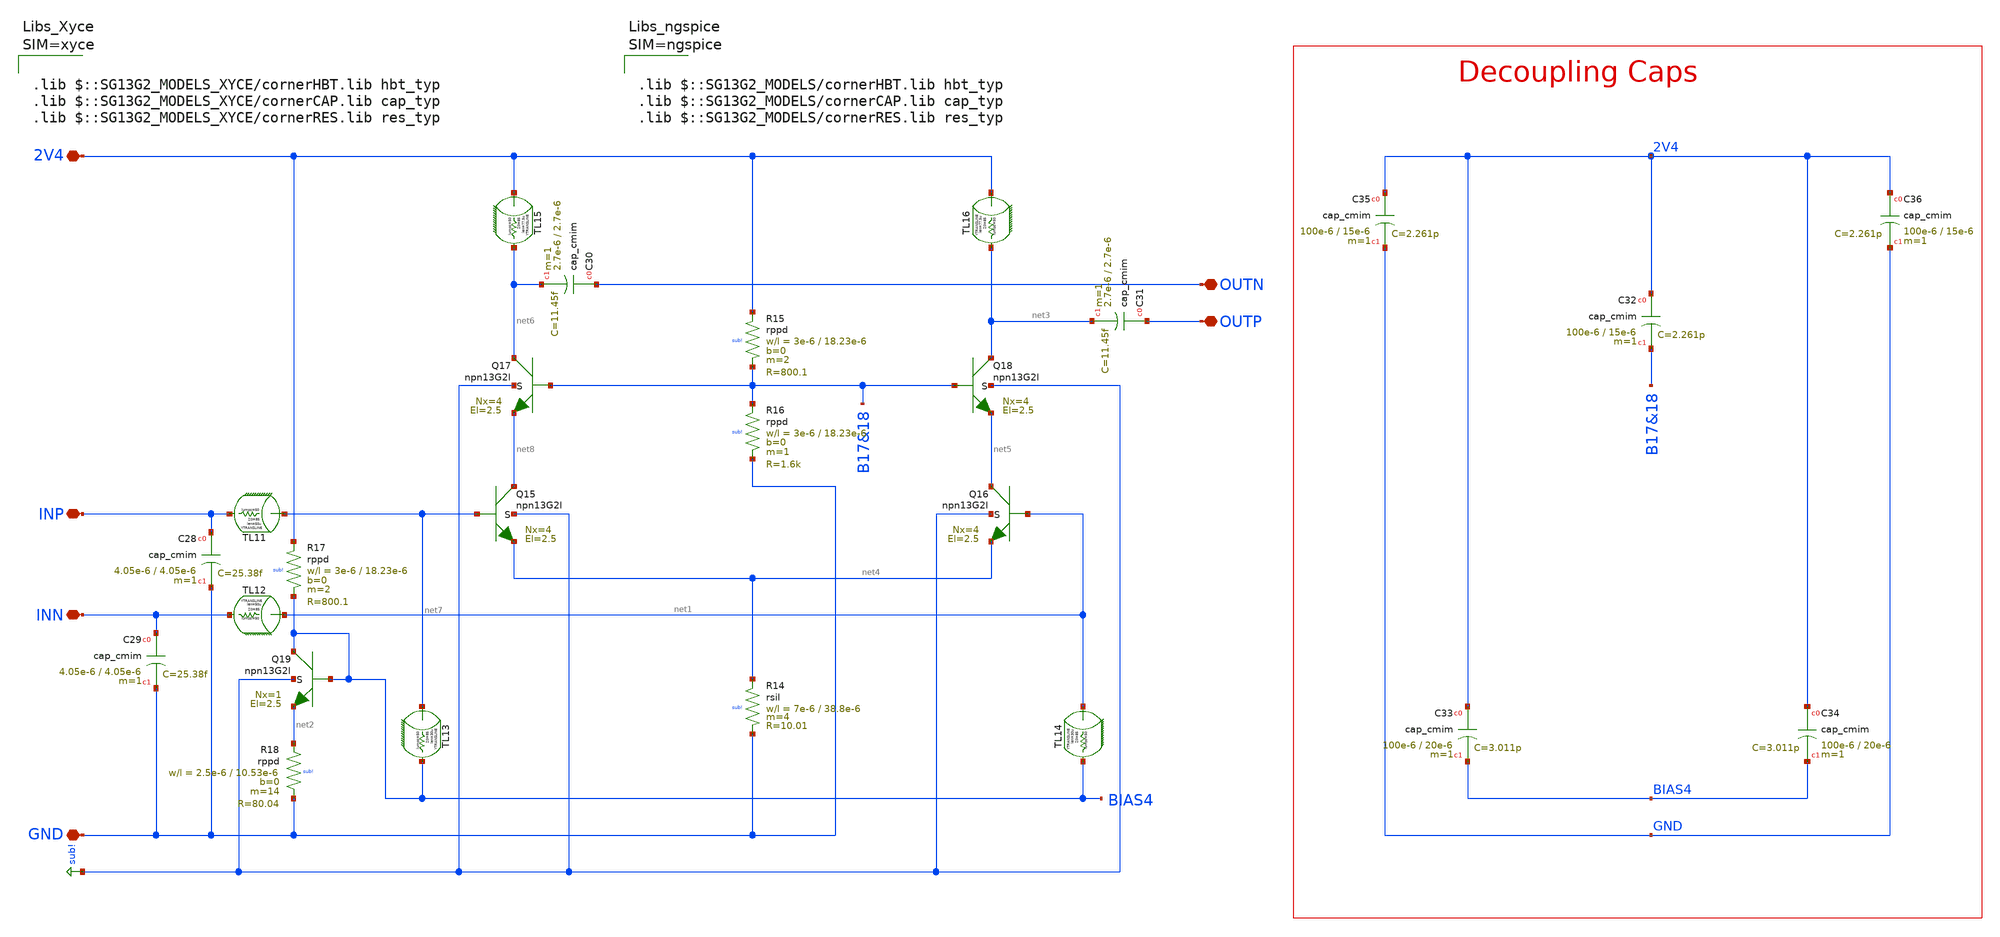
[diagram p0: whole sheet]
** sch_path: mWATTBAT/design_data/xschem/RFAMP_150GD.sch
**.subckt RFAMP_150GD 2V4 GND OUTN OUTP INP INN
*.iopin 2V4
*.iopin GND
*.iopin OUTN
*.iopin OUTP
*.iopin INP
*.iopin INN
XQ15 net8 net7 net4 sub! npn13G2l Nx=4 El=2.5 mm_ok=1
XQ16 net5 net1 net4 sub! npn13G2l Nx=4 El=2.5 mm_ok=1
XQ19 BIAS4 BIAS4 net2 sub! npn13G2l Nx=1 El=2.5 mm_ok=1
XQ17 net6 B17&18 net8 sub! npn13G2l Nx=4 El=2.5 mm_ok=1
XQ18 net3 B17&18 net5 sub! npn13G2l Nx=4 El=2.5 mm_ok=1
ytransline TL13 net7 BIAS4 ytransline_TL13 len=30u lumps=50
.model ytransline_TL13 transline r=22.16k l=445.9n C=61.5p
ytransline TL14 net1 BIAS4 ytransline_TL14 len=30u lumps=50
.model ytransline_TL14 transline r=22.16k l=445.9n C=61.5p
ytransline TL11 net7 INP ytransline_TL11 len=50u lumps=50
.model ytransline_TL11 transline r=22.16k l=445.9n C=61.5p
ytransline TL12 net1 INN ytransline_TL12 len=50u lumps=50
.model ytransline_TL12 transline r=22.16k l=445.9n C=61.5p
ytransline TL15 2V4 net6 ytransline_TL15 len=77.5u lumps=50
.model ytransline_TL15 transline r=22.16k l=445.9n C=61.5p
ytransline TL16 2V4 net3 ytransline_TL16 len=77.5u lumps=50
.model ytransline_TL16 transline r=22.16k l=445.9n C=61.5p
XR17 2V4 BIAS4 sub! rppd w=3e-6 l=18.23e-6 m=2 b=0 mm_ok=1
XC28 INP GND cap_cmim w=4.05e-6 l=4.05e-6 m=1 mm_ok=1
XC29 INN GND cap_cmim w=4.05e-6 l=4.05e-6 m=1 mm_ok=1
XC30 OUTN net6 cap_cmim w=2.7e-6 l=2.7e-6 m=1 mm_ok=1
XC31 OUTP net3 cap_cmim w=2.7e-6 l=2.7e-6 m=1 mm_ok=1
XR18 net2 GND sub! rppd w=2.5e-6 l=10.53e-6 m=14 b=0 mm_ok=1
XR15 2V4 B17&18 sub! rppd w=3e-6 l=18.23e-6 m=2 b=0 mm_ok=1
XR16 B17&18 GND sub! rppd w=3e-6 l=18.23e-6 m=1 b=0 mm_ok=1
XC33 2V4 BIAS4 cap_cmim w=100e-6 l=20e-6 m=1 mm_ok=1
XC32 2V4 B17&18 cap_cmim w=100e-6 l=15e-6 m=1 mm_ok=1
XC34 2V4 BIAS4 cap_cmim w=100e-6 l=20e-6 m=1 mm_ok=1
XC35 2V4 GND cap_cmim w=100e-6 l=15e-6 m=1 mm_ok=1
XC36 2V4 GND cap_cmim w=100e-6 l=15e-6 m=1 mm_ok=1
XR14 net4 GND sub! rsil w=7e-6 l=38.8e-6 m=4 mm_ok=1
**** begin user architecture code






.lib $::SG13G2_MODELS/cornerHBT.lib hbt_typ
.lib $::SG13G2_MODELS/cornerCAP.lib cap_typ
.lib $::SG13G2_MODELS/cornerRES.lib res_typ



**** end user architecture code
**.ends
.GLOBAL sub!
.end
